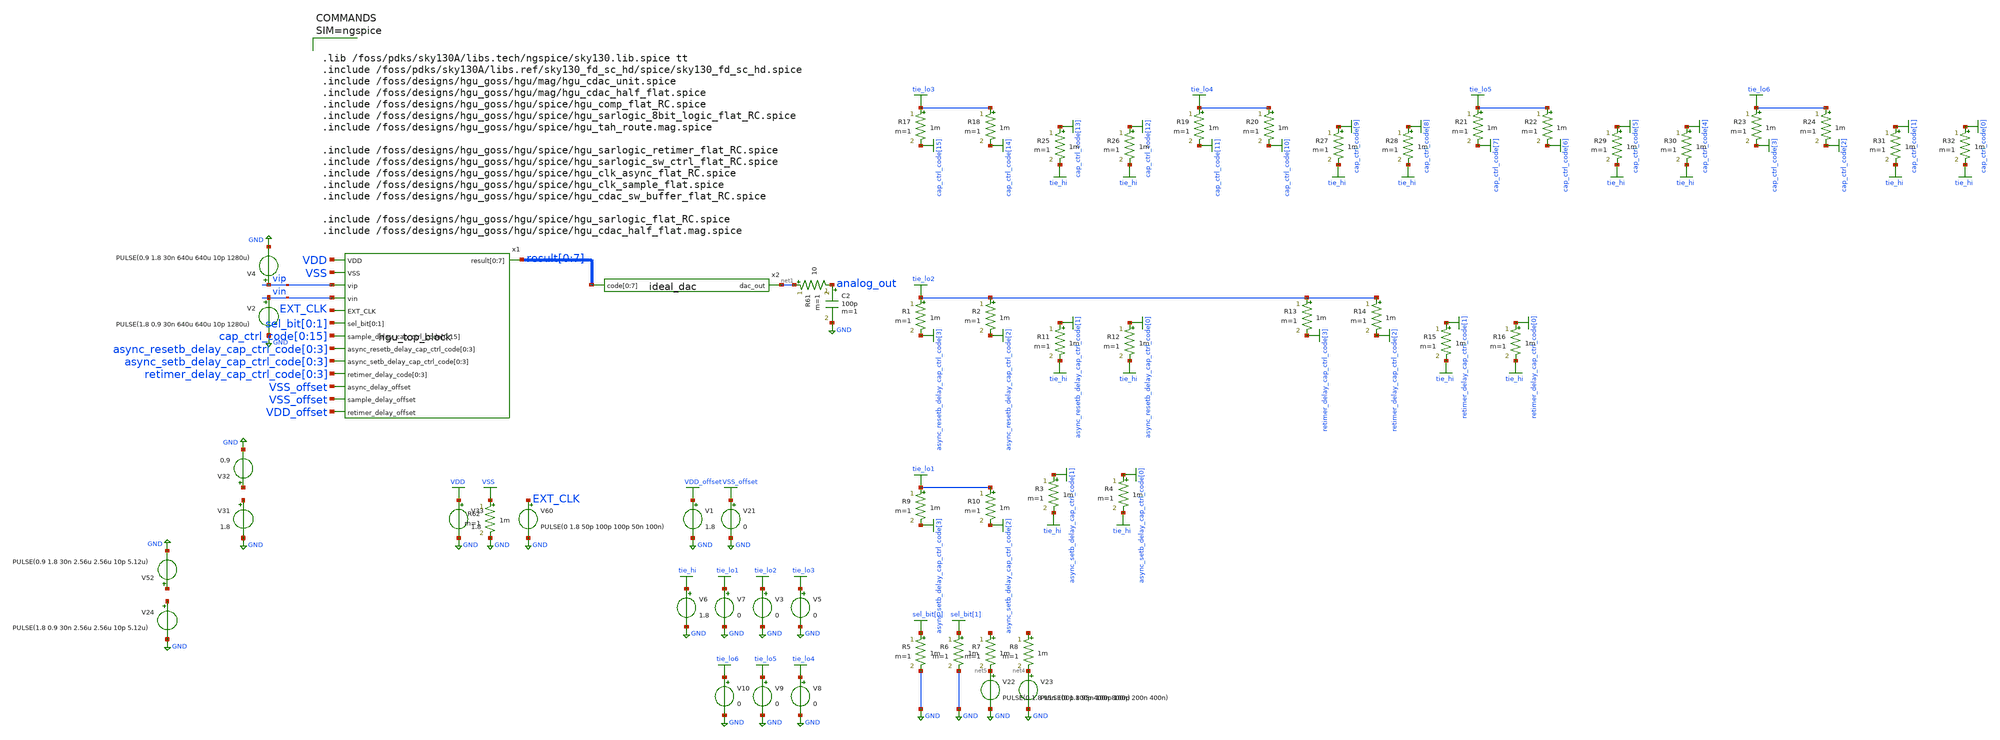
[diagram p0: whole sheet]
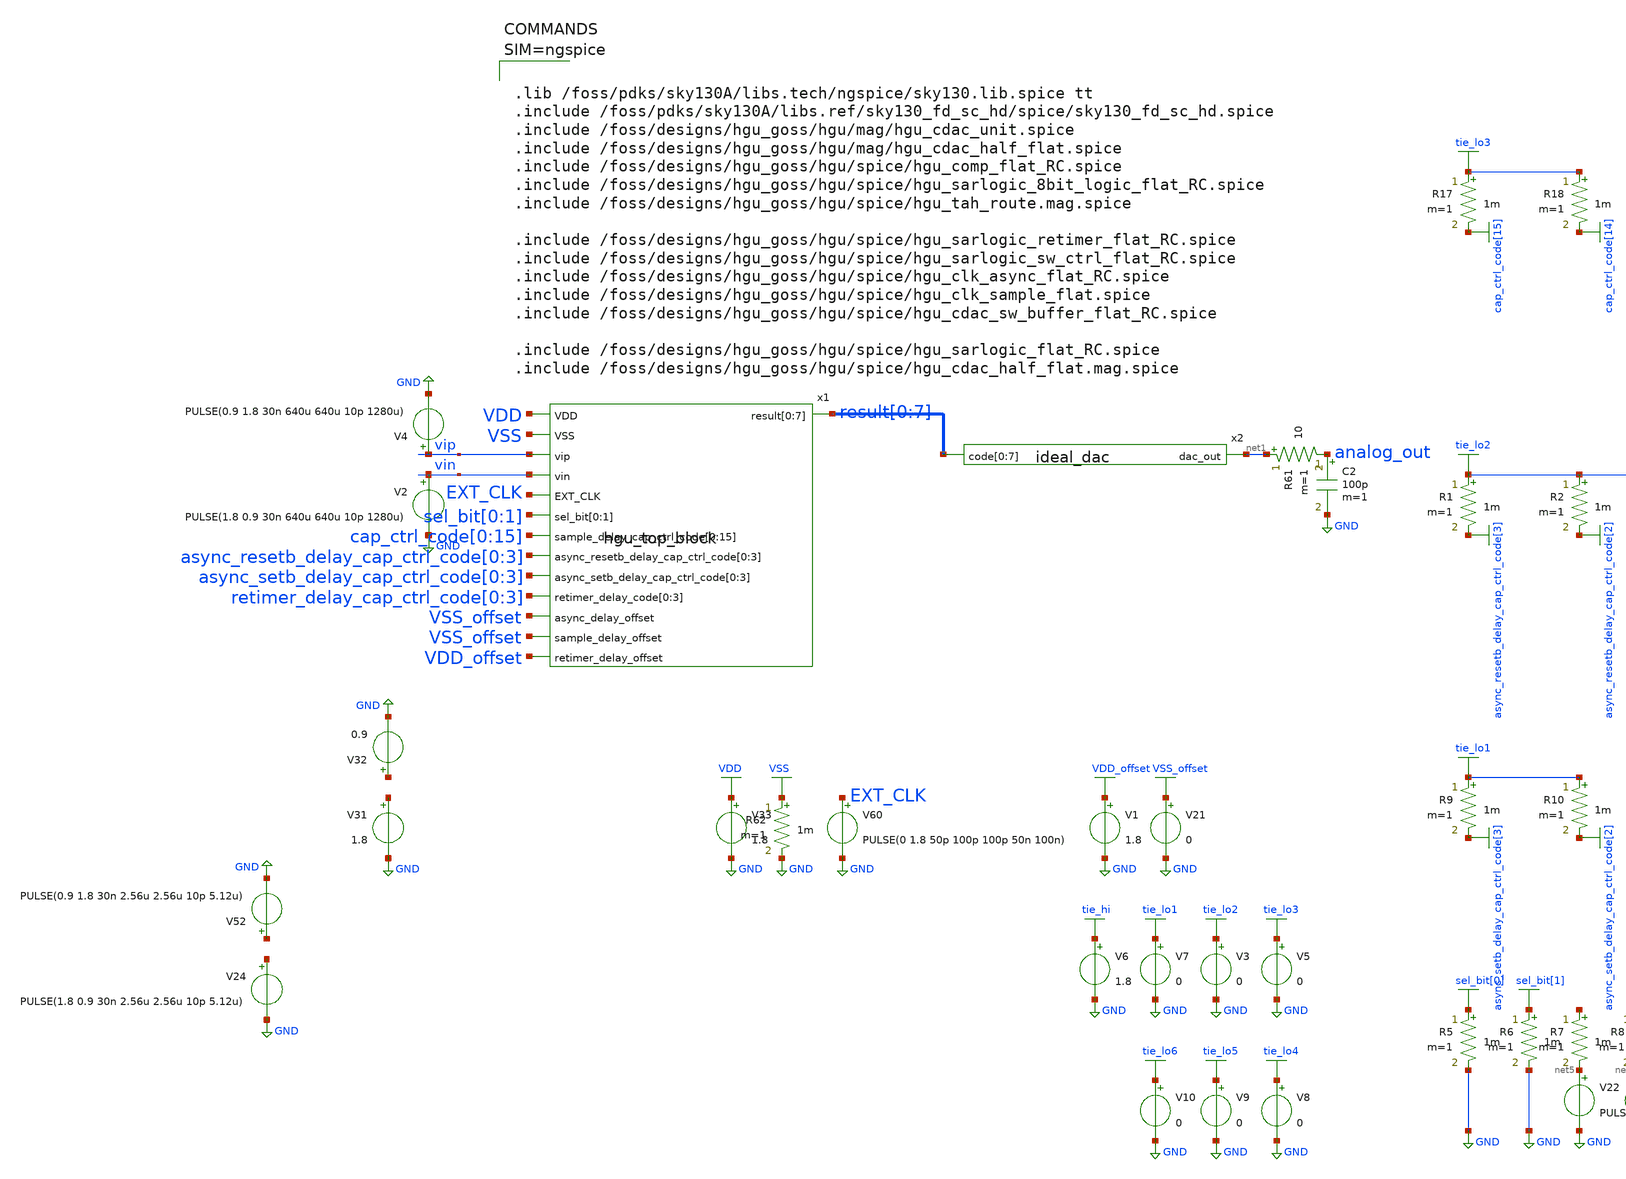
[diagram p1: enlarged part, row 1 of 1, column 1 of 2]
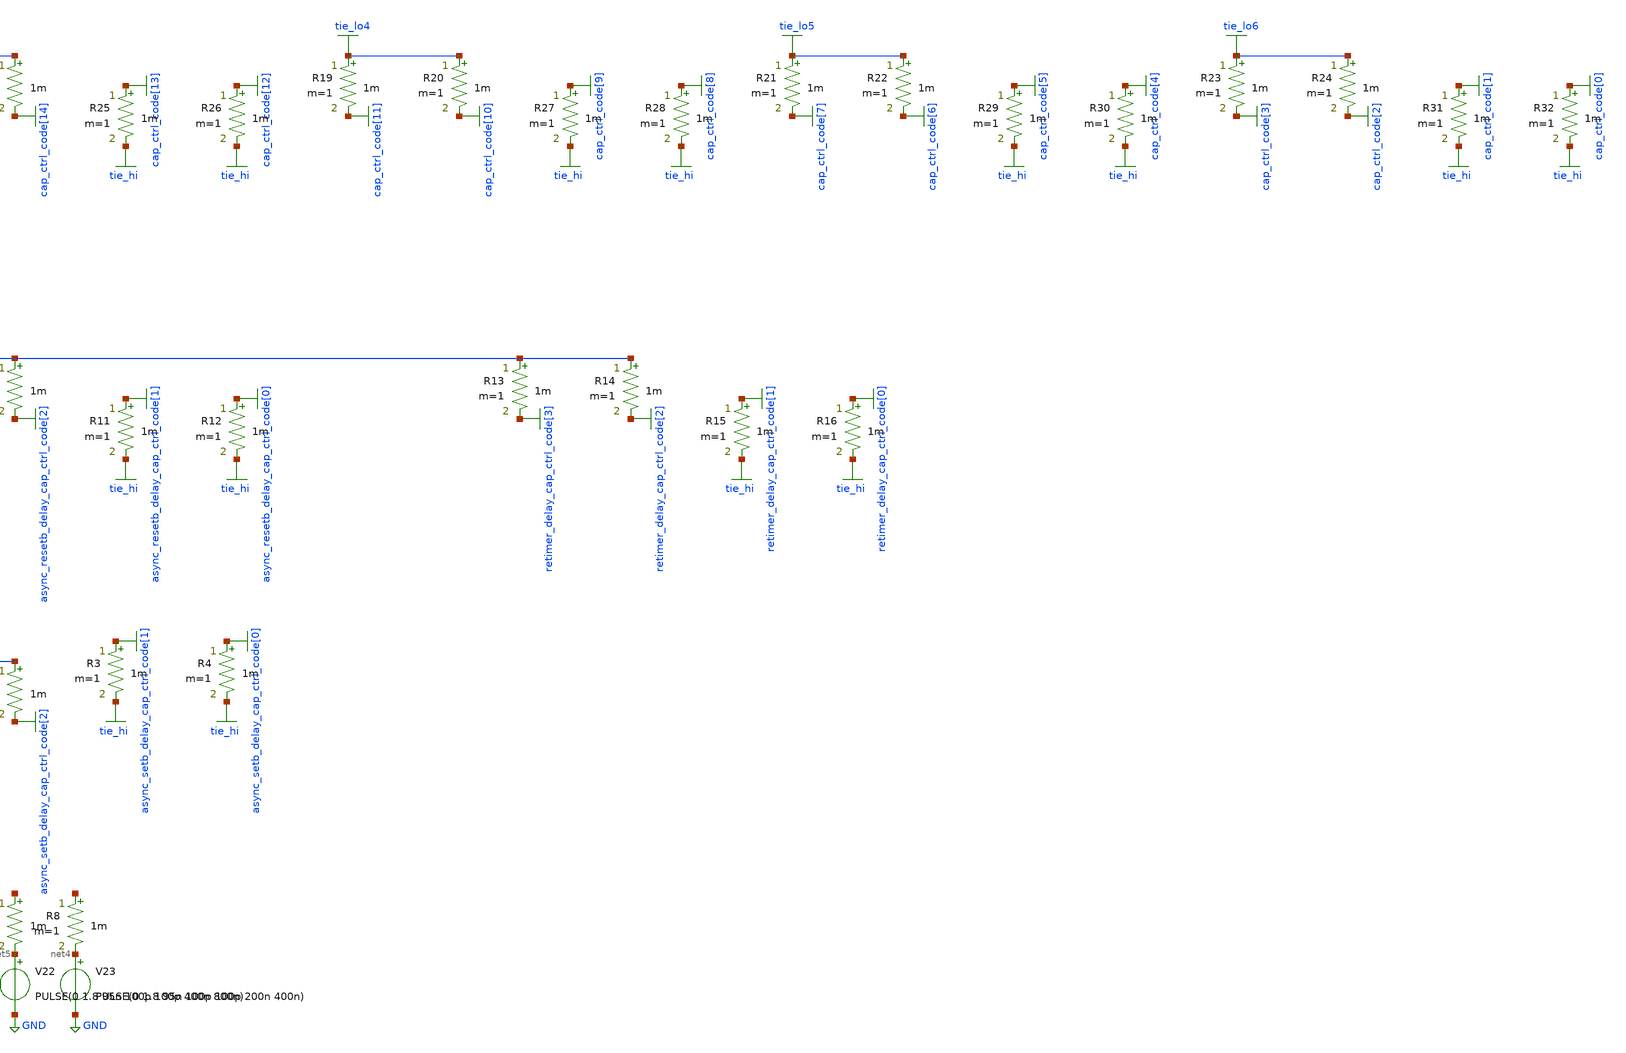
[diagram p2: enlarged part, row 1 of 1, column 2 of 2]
** sch_path: hgu/tb/tb_hgu_top_block.sch
**.subckt tb_hgu_top_block
x1 VDD result[0] result[1] result[2] result[3] result[4] result[5] result[6] result[7] VSS vip vin
+ EXT_CLK sel_bit[0] sel_bit[1] cap_ctrl_code[0] cap_ctrl_code[1] cap_ctrl_code[2] cap_ctrl_code[3]
+ cap_ctrl_code[4] cap_ctrl_code[5] cap_ctrl_code[6] cap_ctrl_code[7] cap_ctrl_code[8] cap_ctrl_code[9]
+ cap_ctrl_code[10] cap_ctrl_code[11] cap_ctrl_code[12] cap_ctrl_code[13] cap_ctrl_code[14] cap_ctrl_code[15]
+ async_resetb_delay_cap_ctrl_code[0] async_resetb_delay_cap_ctrl_code[1] async_resetb_delay_cap_ctrl_code[2]
+ async_resetb_delay_cap_ctrl_code[3] async_setb_delay_cap_ctrl_code[0] async_setb_delay_cap_ctrl_code[1]
+ async_setb_delay_cap_ctrl_code[2] async_setb_delay_cap_ctrl_code[3] retimer_delay_cap_ctrl_code[0] retimer_delay_cap_ctrl_code[1]
+ retimer_delay_cap_ctrl_code[2] retimer_delay_cap_ctrl_code[3] VSS_offset VSS_offset VDD_offset hgu_top_block
C2 analog_out GND 100p m=1
V33 VDD GND 1.8
V31 net2 GND 1.8
V32 net3 GND 0.9
V60 EXT_CLK GND PULSE(0 1.8 50p 100p 100p 50n 100n)
V2 vin GND PULSE(1.8 0.9 30n 640u 640u 10p 1280u)
V4 vip GND PULSE(0.9 1.8 30n 640u 640u 10p 1280u)
V1 VDD_offset GND 1.8
V21 VSS_offset GND 0
V23 net4 GND PULSE(0 1.8 95n 100p 100p 200n 400n)
V22 net5 GND PULSE(0 1.8 95n 100p 100p 400n 800n)
x2 net1 result[0] result[1] result[2] result[3] result[4] result[5] result[6] result[7] ideal_dac
V24 net6 GND PULSE(1.8 0.9 30n 2.56u 2.56u 10p 5.12u)
V52 net7 GND PULSE(0.9 1.8 30n 2.56u 2.56u 10p 5.12u)
R61 net1 analog_out 10 m=1
R62 VSS GND 1m m=1
R3 async_setb_delay_cap_ctrl_code[1] tie_hi 1m m=1
R4 async_setb_delay_cap_ctrl_code[0] tie_hi 1m m=1
R5 sel_bit[0] GND 1m m=1
R6 sel_bit[1] GND 1m m=1
R7 net8 net5 1m m=1
R8 net9 net4 1m m=1
V6 tie_hi GND 1.8
V7 tie_lo1 GND 0
R9 tie_lo1 async_setb_delay_cap_ctrl_code[3] 1m m=1
R10 tie_lo1 async_setb_delay_cap_ctrl_code[2] 1m m=1
R1 tie_lo2 async_resetb_delay_cap_ctrl_code[3] 1m m=1
R2 tie_lo2 async_resetb_delay_cap_ctrl_code[2] 1m m=1
R11 async_resetb_delay_cap_ctrl_code[1] tie_hi 1m m=1
R12 async_resetb_delay_cap_ctrl_code[0] tie_hi 1m m=1
R13 tie_lo2 retimer_delay_cap_ctrl_code[3] 1m m=1
R14 tie_lo2 retimer_delay_cap_ctrl_code[2] 1m m=1
R15 retimer_delay_cap_ctrl_code[1] tie_hi 1m m=1
R16 retimer_delay_cap_ctrl_code[0] tie_hi 1m m=1
R17 tie_lo3 cap_ctrl_code[15] 1m m=1
R18 tie_lo3 cap_ctrl_code[14] 1m m=1
R19 tie_lo4 cap_ctrl_code[11] 1m m=1
R20 tie_lo4 cap_ctrl_code[10] 1m m=1
R21 tie_lo5 cap_ctrl_code[7] 1m m=1
R22 tie_lo5 cap_ctrl_code[6] 1m m=1
R23 tie_lo6 cap_ctrl_code[3] 1m m=1
R24 tie_lo6 cap_ctrl_code[2] 1m m=1
R25 cap_ctrl_code[13] tie_hi 1m m=1
R26 cap_ctrl_code[12] tie_hi 1m m=1
R27 cap_ctrl_code[9] tie_hi 1m m=1
R28 cap_ctrl_code[8] tie_hi 1m m=1
R29 cap_ctrl_code[5] tie_hi 1m m=1
R30 cap_ctrl_code[4] tie_hi 1m m=1
R31 cap_ctrl_code[1] tie_hi 1m m=1
R32 cap_ctrl_code[0] tie_hi 1m m=1
V3 tie_lo2 GND 0
V5 tie_lo3 GND 0
V8 tie_lo4 GND 0
V9 tie_lo5 GND 0
V10 tie_lo6 GND 0
**** begin user architecture code



.lib /foss/pdks/sky130A/libs.tech/ngspice/sky130.lib.spice tt
.include /foss/pdks/sky130A/libs.ref/sky130_fd_sc_hd/spice/sky130_fd_sc_hd.spice
.include /foss/designs/hgu_goss/hgu/mag/hgu_cdac_unit.spice
.include /foss/designs/hgu_goss/hgu/mag/hgu_cdac_half_flat.spice
.include /foss/designs/hgu_goss/hgu/spice/hgu_comp_flat_RC.spice
.include /foss/designs/hgu_goss/hgu/spice/hgu_sarlogic_8bit_logic_flat_RC.spice
.include /foss/designs/hgu_goss/hgu/spice/hgu_tah_route.mag.spice

.include /foss/designs/hgu_goss/hgu/spice/hgu_sarlogic_retimer_flat_RC.spice
.include /foss/designs/hgu_goss/hgu/spice/hgu_sarlogic_sw_ctrl_flat_RC.spice
.include /foss/designs/hgu_goss/hgu/spice/hgu_clk_async_flat_RC.spice
.include /foss/designs/hgu_goss/hgu/spice/hgu_clk_sample_flat.spice
.include /foss/designs/hgu_goss/hgu/spice/hgu_cdac_sw_buffer_flat_RC.spice

.include /foss/designs/hgu_goss/hgu/spice/hgu_sarlogic_flat_RC.spice
.include /foss/designs/hgu_goss/hgu/spice/hgu_cdac_half_flat.mag.spice






.OPTIONS savecurrents

.tran 70ps 80us 40us

.option ABSTOL=1e-9 RELTOL=1e-2

.control
	run
	plot analog_out

	wrdata sar_dnl_640u_70ps(040u_080u) x1.sample_clk vip vin analog_out

.endc
*.save x1.sample_clk vip vin x1.tah_vp x1.tah_vn "result[0]" "result[1]" "result[2]" "result[3]" "result[4]" "result[5]" "result[6]" "result[7]" "x1.x1.sar_result_temp[0]" "x1.x1.sar_result_temp[1]" "x1.x1.sar_result_temp[2]" "x1.x1.sar_result_temp[3]" "x1.x1.sar_result_temp[4]" "x1.x1.sar_result_temp[5]" "x1.x1.sar_result_temp[6]" "x1.x1.sar_result_temp[7]"
*.save "x1.result_sw[1]" "x1.result_sw[2]" "x1.result_sw[3]" "x1.result_sw[4]" "x1.result_sw[5]" "x1.result_sw[6]" "x1.result_sw[7]"
*.save "x1.result2_sw[1]" "x1.result2_sw[2]" "x1.result2_sw[3]" "x1.result2_sw[4]" "x1.result2_sw[5]" "x1.result2_sw[6]" "x1.result2_sw[7]"
*.save "x1.result_sw_b[1]" "x1.result_sw_b[2]" "x1.result_sw_b[3]" "x1.result_sw_b[4]" "x1.result_sw_b[5]" "x1.result_sw_b[6]" "x1.result_sw_b[7]"
*.save "x1.result2_sw_b[1]" "x1.result2_sw_b[2]" "x1.result2_sw_b[3]" "x1.result2_sw_b[4]" "x1.result2_sw_b[5]" "x1.result2_sw_b[6]" "x1.result2_sw_b[7]"
*.save x1.comp_result
*.save vdd i(v33) i(v58) i(v59)
*.save ext_clk
*.save "sel_bit[0]" "sel_bit[1]"

*.save x1.sample_clk vip vin x1.tah_vp x1.tah_vn "result[0]" "result[1]" "result[2]" "result[3]" "result[4]" "result[5]" "result[6]" "result[7]"

*.save all

.save x1.sample_clk vip vin analog_out i(v33)


**** end user architecture code
**.ends
.GLOBAL cap_ctrl_code[15]
.GLOBAL cap_ctrl_code[14]
.GLOBAL cap_ctrl_code[13]
.GLOBAL cap_ctrl_code[12]
.GLOBAL cap_ctrl_code[11]
.GLOBAL cap_ctrl_code[10]
.GLOBAL cap_ctrl_code[9]
.GLOBAL cap_ctrl_code[8]
.GLOBAL GND
.GLOBAL async_resetb_delay_cap_ctrl_code[3]
.GLOBAL async_resetb_delay_cap_ctrl_code[2]
.GLOBAL async_resetb_delay_cap_ctrl_code[1]
.GLOBAL async_resetb_delay_cap_ctrl_code[0]
.GLOBAL async_setb_delay_cap_ctrl_code[3]
.GLOBAL async_setb_delay_cap_ctrl_code[2]
.GLOBAL async_setb_delay_cap_ctrl_code[1]
.GLOBAL async_setb_delay_cap_ctrl_code[0]
.GLOBAL cap_ctrl_code[7]
.GLOBAL cap_ctrl_code[6]
.GLOBAL cap_ctrl_code[5]
.GLOBAL cap_ctrl_code[4]
.GLOBAL cap_ctrl_code[3]
.GLOBAL cap_ctrl_code[2]
.GLOBAL cap_ctrl_code[1]
.GLOBAL cap_ctrl_code[0]
.GLOBAL retimer_delay_cap_ctrl_code[3]
.GLOBAL retimer_delay_cap_ctrl_code[2]
.GLOBAL retimer_delay_cap_ctrl_code[1]
.GLOBAL retimer_delay_cap_ctrl_code[0]
.GLOBAL VDD
.GLOBAL VSS
.GLOBAL VDD_offset
.GLOBAL VSS_offset
.GLOBAL sel_bit[1]
.GLOBAL sel_bit[0]
.GLOBAL tie_hi
.GLOBAL tie_lo1
.GLOBAL tie_lo2
.GLOBAL tie_lo3
.GLOBAL tie_lo5
.GLOBAL tie_lo4
.GLOBAL tie_lo6
.end
